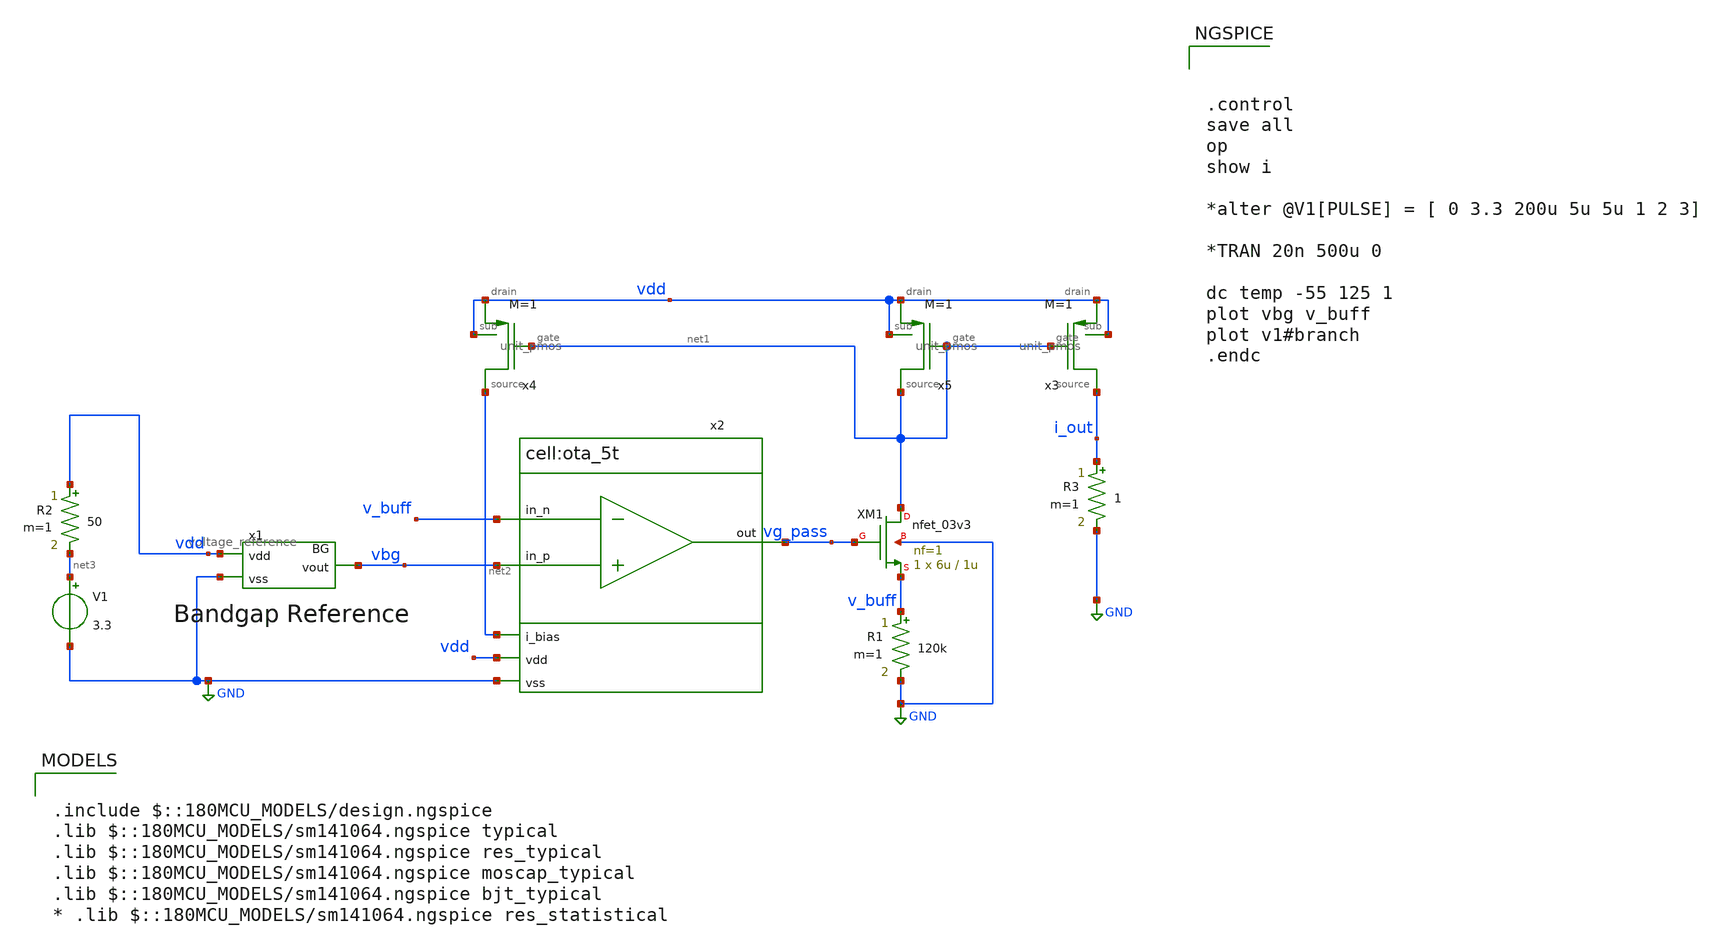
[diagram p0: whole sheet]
** sch_path: designs/libs/tb_analog/vref/vref_tb.sch
* designs/libs/core_analog/vref/voltage_reference.sch:
* by Harald Pretl under the Apache License 2.0.
**.subckt vref_tb
V1 net3 GND 3.3
x1 vdd vbg GND voltage_reference
x3 vdd vdd net1 i_out unit_pmos M=1
R1 v_buff GND 120k m=1
x4 vdd vdd net1 net2 unit_pmos M=1
x2 vdd vg_pass vbg v_buff net2 GND ota_5t
XM1 net1 vg_pass v_buff GND nfet_03v3 L=1u W=6u nf=1 ad='int((nf+1)/2) * W/nf * 0.18u' as='int((nf+2)/2) * W/nf * 0.18u'
+ pd='2*int((nf+1)/2) * (W/nf + 0.18u)' ps='2*int((nf+2)/2) * (W/nf + 0.18u)' nrd='0.18u / W' nrs='0.18u / W'
+ sa=0 sb=0 sd=0 m=1
x5 vdd vdd net1 net1 unit_pmos M=1
R2 vdd net3 50 m=1
R3 i_out GND 1 m=1
**** begin user architecture code



.control
save all
op
show i

*alter @V1[PULSE] = [ 0 3.3 200u 5u 5u 1 2 3]

*TRAN 20n 500u 0

dc temp -55 125 1
plot vbg v_buff
plot v1#branch
.endc



.include $::180MCU_MODELS/design.ngspice
.lib $::180MCU_MODELS/sm141064.ngspice typical
.lib $::180MCU_MODELS/sm141064.ngspice res_typical
.lib $::180MCU_MODELS/sm141064.ngspice moscap_typical
.lib $::180MCU_MODELS/sm141064.ngspice bjt_typical
* .lib $::180MCU_MODELS/sm141064.ngspice res_statistical

**** end user architecture code
**.ends

* expanding   symbol:  libs/core_analog/vref/voltage_reference.sym # of pins=3
** sym_path: libs/core_analog/vref/voltage_reference.sym
** sch_path: libs/core_analog/vref/voltage_reference.sch
.subckt voltage_reference vdd vout vss
*.ipin vdd
*.opin vout
*.ipin vss
XM1B vg1 vg2 net4 vss nfet_03v3 L=1u W=5u nf=1 ad='int((nf+1)/2) * W/nf * 0.18u' as='int((nf+2)/2) * W/nf * 0.18u'
+ pd='2*int((nf+1)/2) * (W/nf + 0.18u)' ps='2*int((nf+2)/2) * (W/nf + 0.18u)' nrd='0.18u / W' nrs='0.18u / W'
+ sa=0 sb=0 sd=0 m=1
XM1A net4 vg1 vb1 vss nfet_03v3 L=1u W=5u nf=1 ad='int((nf+1)/2) * W/nf * 0.18u' as='int((nf+2)/2) * W/nf * 0.18u'
+ pd='2*int((nf+1)/2) * (W/nf + 0.18u)' ps='2*int((nf+2)/2) * (W/nf + 0.18u)' nrd='0.18u / W' nrs='0.18u / W'
+ sa=0 sb=0 sd=0 m=1
XM2B vg3 vg2 net1 vss nfet_03v3 L=1u W=5u nf=1 ad='int((nf+1)/2) * W/nf * 0.18u' as='int((nf+2)/2) * W/nf * 0.18u'
+ pd='2*int((nf+1)/2) * (W/nf + 0.18u)' ps='2*int((nf+2)/2) * (W/nf + 0.18u)' nrd='0.18u / W' nrs='0.18u / W'
+ sa=0 sb=0 sd=0 m=1
XM2A net1 vg1 v2_match vss nfet_03v3 L=1u W=5u nf=1 ad='int((nf+1)/2) * W/nf * 0.18u' as='int((nf+2)/2) * W/nf * 0.18u'
+ pd='2*int((nf+1)/2) * (W/nf + 0.18u)' ps='2*int((nf+2)/2) * (W/nf + 0.18u)' nrd='0.18u / W' nrs='0.18u / W'
+ sa=0 sb=0 sd=0 m=1
XM4A vg4 vg3 net5 vdd pfet_03v3 L=1u W=15u nf=3 ad='int((nf+1)/2) * W/nf * 0.18u' as='int((nf+2)/2) * W/nf * 0.18u'
+ pd='2*int((nf+1)/2) * (W/nf + 0.18u)' ps='2*int((nf+2)/2) * (W/nf + 0.18u)' nrd='0.18u / W' nrs='0.18u / W'
+ sa=0 sb=0 sd=0 m=1
XM4B net5 vg4 vdd vdd pfet_03v3 L=1u W=15u nf=3 ad='int((nf+1)/2) * W/nf * 0.18u' as='int((nf+2)/2) * W/nf * 0.18u'
+ pd='2*int((nf+1)/2) * (W/nf + 0.18u)' ps='2*int((nf+2)/2) * (W/nf + 0.18u)' nrd='0.18u / W' nrs='0.18u / W'
+ sa=0 sb=0 sd=0 m=1
XM3A vg2 vg3 net3 vdd pfet_03v3 L=1u W=15u nf=3 ad='int((nf+1)/2) * W/nf * 0.18u' as='int((nf+2)/2) * W/nf * 0.18u'
+ pd='2*int((nf+1)/2) * (W/nf + 0.18u)' ps='2*int((nf+2)/2) * (W/nf + 0.18u)' nrd='0.18u / W' nrs='0.18u / W'
+ sa=0 sb=0 sd=0 m=1
XM3B net3 vg4 vdd vdd pfet_03v3 L=1u W=15u nf=3 ad='int((nf+1)/2) * W/nf * 0.18u' as='int((nf+2)/2) * W/nf * 0.18u'
+ pd='2*int((nf+1)/2) * (W/nf + 0.18u)' ps='2*int((nf+2)/2) * (W/nf + 0.18u)' nrd='0.18u / W' nrs='0.18u / W'
+ sa=0 sb=0 sd=0 m=1
XM5A vout vg3 net2 vdd pfet_03v3 L=1u W=15u nf=3 ad='int((nf+1)/2) * W/nf * 0.18u' as='int((nf+2)/2) * W/nf * 0.18u'
+ pd='2*int((nf+1)/2) * (W/nf + 0.18u)' ps='2*int((nf+2)/2) * (W/nf + 0.18u)' nrd='0.18u / W' nrs='0.18u / W'
+ sa=0 sb=0 sd=0 m=1
XM5B net2 vg4 vdd vdd pfet_03v3 L=1u W=15u nf=3 ad='int((nf+1)/2) * W/nf * 0.18u' as='int((nf+2)/2) * W/nf * 0.18u'
+ pd='2*int((nf+1)/2) * (W/nf + 0.18u)' ps='2*int((nf+2)/2) * (W/nf + 0.18u)' nrd='0.18u / W' nrs='0.18u / W'
+ sa=0 sb=0 sd=0 m=1
XQ11 vss vss vb2 pnp_10p00x00p42 m=1 par=1
XQ12 vss vss vb2 pnp_10p00x00p42 m=1 par=1
XQ13 vss vss vb2 pnp_10p00x00p42 m=1 par=1
XQ14 vss vss vb2 pnp_10p00x00p42 m=1 par=1
XQ15 vss vss vb2 pnp_10p00x00p42 m=1 par=1
XQ16 vss vss vb2 pnp_10p00x00p42 m=1 par=1
XQ17 vss vss vb2 pnp_10p00x00p42 m=1 par=1
XQ18 vss vss vb2 pnp_10p00x00p42 m=1 par=1
XQ21 vss vss vb3 pnp_10p00x00p42 m=1 par=1
XQ22 vss vss vb3 pnp_10p00x00p42 m=1 par=1
XQ23 vss vss vb3 pnp_10p00x00p42 m=1 par=1
XQ24 vss vss vb3 pnp_10p00x00p42 m=1 par=1
XQ25 vss vss vb3 pnp_10p00x00p42 m=1 par=1
XQ26 vss vss vb3 pnp_10p00x00p42 m=1 par=1
XQ27 vss vss vb3 pnp_10p00x00p42 m=1 par=1
XQ28 vss vss vb3 pnp_10p00x00p42 m=1 par=1
XQ31 vss vss vb1 pnp_10p00x00p42 m=1 par=1
XQ32 vss vss vb1 pnp_10p00x00p42 m=1 par=1
XM1 vg2 vg2 vg3 vdd pfet_03v3 L=10u W=0.4u nf=1 ad='int((nf+1)/2) * W/nf * 0.18u' as='int((nf+2)/2) * W/nf * 0.18u'
+ pd='2*int((nf+1)/2) * (W/nf + 0.18u)' ps='2*int((nf+2)/2) * (W/nf + 0.18u)' nrd='0.18u / W' nrs='0.18u / W'
+ sa=0 sb=0 sd=0 m=1
XR3 vg3 vg4 vss ppolyf_u r_width=1e-6 r_length=15e-6 m=1
XR5 vg1 vg2 vss ppolyf_u r_width=1e-6 r_length=15e-6 m=1
x1 vout vss vb3 vref_R2
x2 v2_match vss vb2 vref_R1
.ends


* expanding   symbol:  libs/core_analog/unit_pmos/unit_pmos.sym # of pins=4
** sym_path: libs/core_analog/unit_pmos/unit_pmos.sym
** sch_path: libs/core_analog/unit_pmos/unit_pmos.sch
.subckt unit_pmos drain sub gate source
*.iopin drain
*.iopin source
*.iopin sub
*.iopin gate
**** begin user architecture code

.param M=1

**** end user architecture code
XM3 drain gate source sub pfet_03v3 L=1u W=3.5u nf=1 ad='int((nf+1)/2) * W/nf * 0.18u' as='int((nf+2)/2) * W/nf * 0.18u'
+ pd='2*int((nf+1)/2) * (W/nf + 0.18u)' ps='2*int((nf+2)/2) * (W/nf + 0.18u)' nrd='0.18u / W' nrs='0.18u / W'
+ sa=0 sb=0 sd=0 m={M}
.ends


* expanding   symbol:  libs/core_analog/ota_5t/ota_5t.sym # of pins=6
** sym_path: libs/core_analog/ota_5t/ota_5t.sym
** sch_path: libs/core_analog/ota_5t/ota_5t.sch
.subckt ota_5t vdd out in_p in_n i_bias vss
*.ipin in_p
*.ipin in_n
*.ipin i_bias
*.ipin vdd
*.ipin vss
*.opin out
XM1 net2 i_bias vss vss nfet_03v3 L=1u W=2.5u nf=1 ad='int((nf+1)/2) * W/nf * 0.18u' as='int((nf+2)/2) * W/nf * 0.18u'
+ pd='2*int((nf+1)/2) * (W/nf + 0.18u)' ps='2*int((nf+2)/2) * (W/nf + 0.18u)' nrd='0.18u / W' nrs='0.18u / W'
+ sa=0 sb=0 sd=0 m=1
XM2 i_bias i_bias vss vss nfet_03v3 L=1u W=2.5u nf=1 ad='int((nf+1)/2) * W/nf * 0.18u' as='int((nf+2)/2) * W/nf * 0.18u'
+ pd='2*int((nf+1)/2) * (W/nf + 0.18u)' ps='2*int((nf+2)/2) * (W/nf + 0.18u)' nrd='0.18u / W' nrs='0.18u / W'
+ sa=0 sb=0 sd=0 m=1
XM3 net1 in_p net2 vss nfet_03v3 L=1u W=4.5u nf=2 ad='int((nf+1)/2) * W/nf * 0.18u' as='int((nf+2)/2) * W/nf * 0.18u'
+ pd='2*int((nf+1)/2) * (W/nf + 0.18u)' ps='2*int((nf+2)/2) * (W/nf + 0.18u)' nrd='0.18u / W' nrs='0.18u / W'
+ sa=0 sb=0 sd=0 m=1
XM4 out in_n net2 vss nfet_03v3 L=1u W=4.5u nf=2 ad='int((nf+1)/2) * W/nf * 0.18u' as='int((nf+2)/2) * W/nf * 0.18u'
+ pd='2*int((nf+1)/2) * (W/nf + 0.18u)' ps='2*int((nf+2)/2) * (W/nf + 0.18u)' nrd='0.18u / W' nrs='0.18u / W'
+ sa=0 sb=0 sd=0 m=1
XM5 out net1 vdd vdd pfet_03v3 L=1u W=5.5u nf=1 ad='int((nf+1)/2) * W/nf * 0.18u' as='int((nf+2)/2) * W/nf * 0.18u'
+ pd='2*int((nf+1)/2) * (W/nf + 0.18u)' ps='2*int((nf+2)/2) * (W/nf + 0.18u)' nrd='0.18u / W' nrs='0.18u / W'
+ sa=0 sb=0 sd=0 m=1
XM6 net1 net1 vdd vdd pfet_03v3 L=1u W=5.5u nf=1 ad='int((nf+1)/2) * W/nf * 0.18u' as='int((nf+2)/2) * W/nf * 0.18u'
+ pd='2*int((nf+1)/2) * (W/nf + 0.18u)' ps='2*int((nf+2)/2) * (W/nf + 0.18u)' nrd='0.18u / W' nrs='0.18u / W'
+ sa=0 sb=0 sd=0 m=1
.ends


* expanding   symbol:  libs/core_analog/vref/vref_R2.sym # of pins=3
** sym_path: designs/libs/core_analog/vref/vref_R2.sym
** sch_path: designs/libs/core_analog/vref/vref_R2.sch
.subckt vref_R2 r_p b r_n
*.iopin r_p
*.iopin r_n
*.iopin b
XR1 net1 net3 b ppolyf_u r_width=2.5e-6 r_length=25e-6 m=1
XR2 net2 net4 b ppolyf_u r_width=2.5e-6 r_length=25e-6 m=1
XR3 r_n net1 b ppolyf_u r_width=2.5e-6 r_length=25e-6 m=1
XR4 net3 net2 b ppolyf_u r_width=2.5e-6 r_length=25e-6 m=1
XR5 net5 net6 b ppolyf_u r_width=2.5e-6 r_length=25e-6 m=1
XR7 net4 net5 b ppolyf_u r_width=2.5e-6 r_length=25e-6 m=1
XR8 net6 net12 b ppolyf_u r_width=2.5e-6 r_length=25e-6 m=1
XR6 net12 net7 b ppolyf_u r_width=2.5e-6 r_length=25e-6 m=1
XR9 net8 net10 b ppolyf_u r_width=2.5e-6 r_length=25e-6 m=1
XR10 net9 net11 b ppolyf_u r_width=2.5e-6 r_length=25e-6 m=1
XR11 net7 net8 b ppolyf_u r_width=2.5e-6 r_length=25e-6 m=1
XR12 net10 net9 b ppolyf_u r_width=2.5e-6 r_length=25e-6 m=1
XR13 net11 r_p b ppolyf_u r_width=2.5e-6 r_length=25e-6 m=1
.ends


* expanding   symbol:  libs/core_analog/vref/vref_R1.sym # of pins=3
** sym_path: designs/libs/core_analog/vref/vref_R1.sym
** sch_path: designs/libs/core_analog/vref/vref_R1.sch
.subckt vref_R1 r_p b r_n
*.iopin r_p
*.iopin r_n
*.iopin b
XR1 net1 r_p b ppolyf_u r_width=2.5e-6 r_length=25e-6 m=1
XR2 net2 r_p b ppolyf_u r_width=2.5e-6 r_length=25e-6 m=1
XR3 r_n net1 b ppolyf_u r_width=2.5e-6 r_length=25e-6 m=1
XR4 r_n net2 b ppolyf_u r_width=2.5e-6 r_length=25e-6 m=1
.ends

.GLOBAL GND
.end
